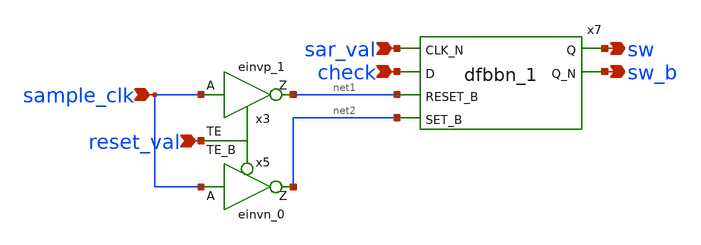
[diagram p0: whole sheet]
** sch_path: module/top_comp_sar/top_comp_sar_parasitic/adc_val_to_sw_ctrl.sch
**.subckt adc_val_to_sw_ctrl sw sw_b sample_clk sar_val reset_val check
*.opin sw
*.opin sw_b
*.ipin sample_clk
*.ipin sar_val
*.ipin reset_val
*.ipin check
x5 sample_clk reset_val VGND VNB VPB VPWR net2 sky130_fd_sc_hd__einvn_0
x3 sample_clk reset_val VGND VNB VPB VPWR net1 sky130_fd_sc_hd__einvp_1
x7 sar_val check net1 net2 VGND VNB VPB VPWR sw sw_b sky130_fd_sc_hd__dfbbn_1
**.ends
.end
